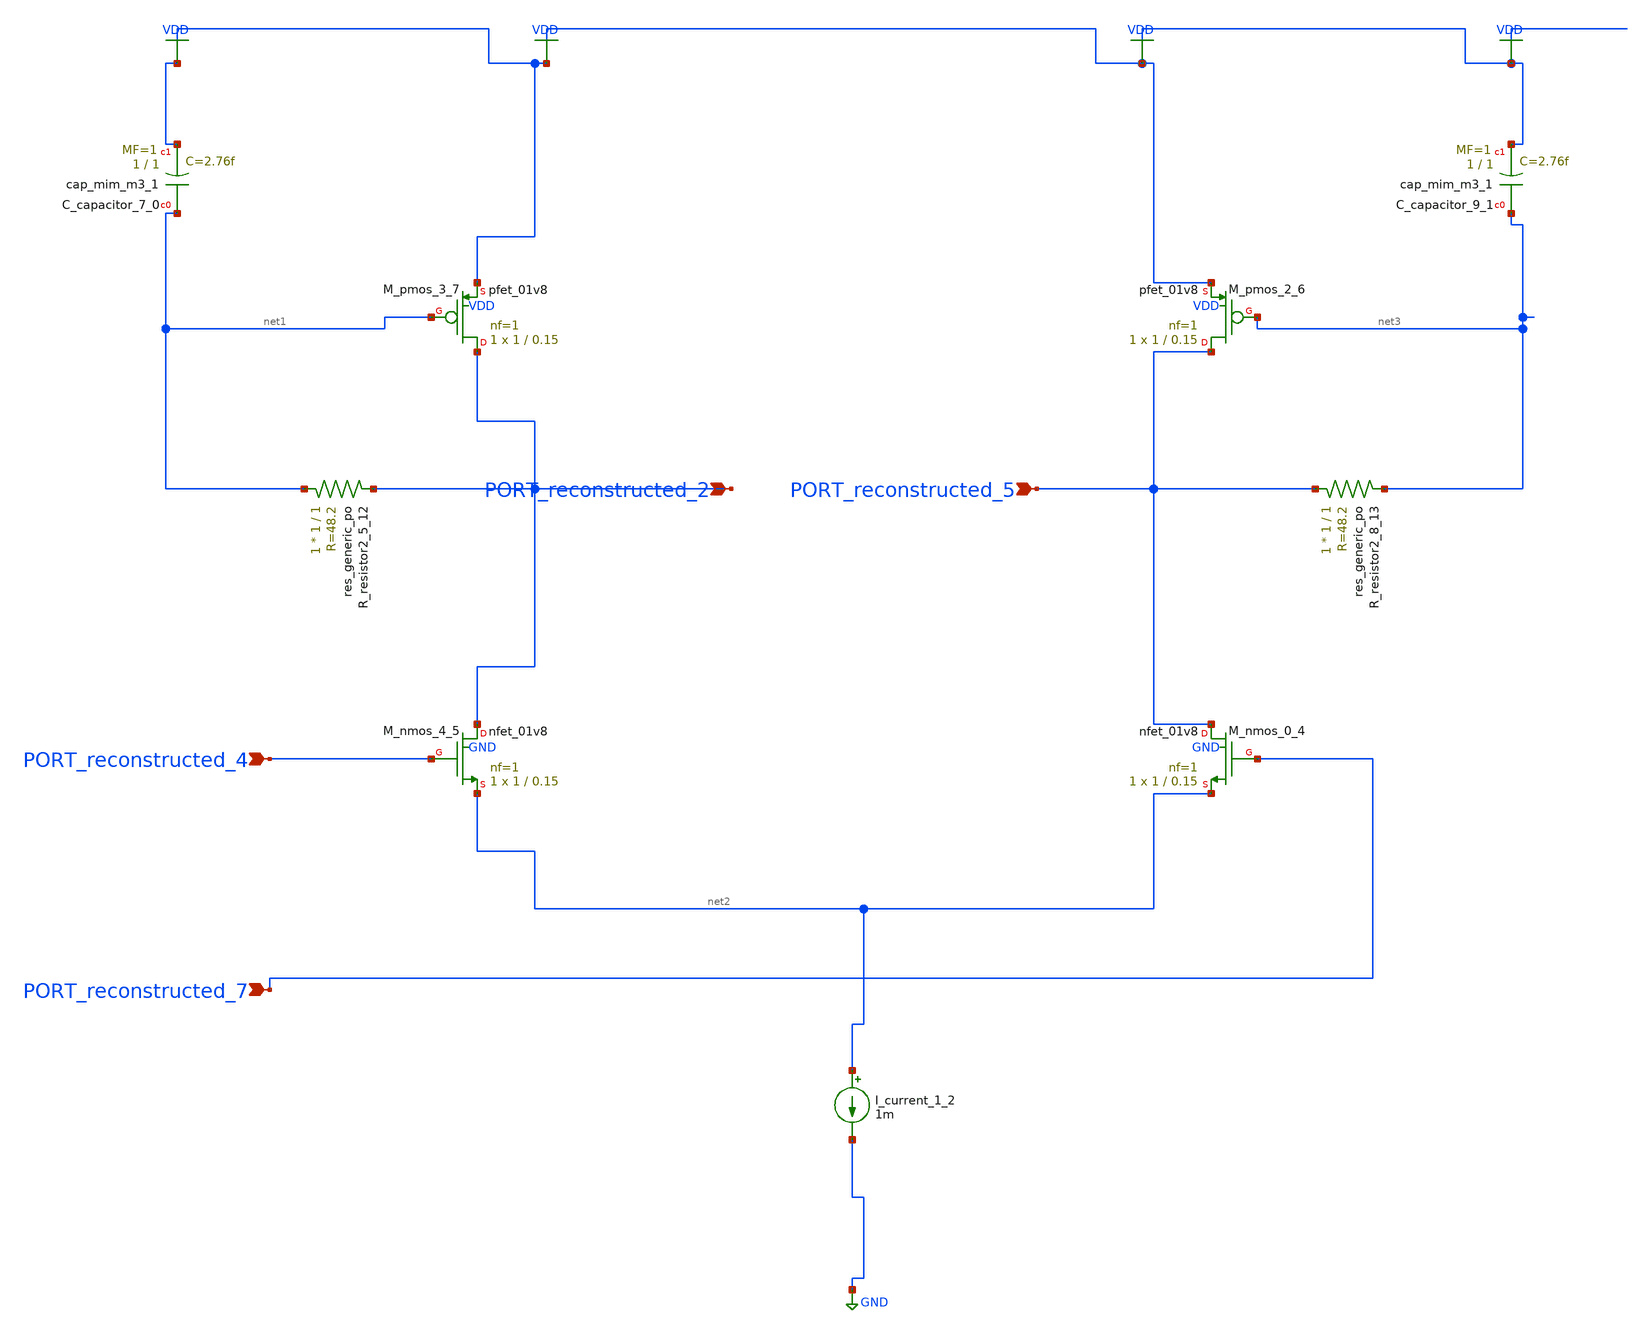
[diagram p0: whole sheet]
** sch_path: schematics/AMSNet/426.sch
**.subckt 426 PORT_reconstructed_2 PORT_reconstructed_5 PORT_reconstructed_4 PORT_reconstructed_7
*.ipin PORT_reconstructed_2
*.ipin PORT_reconstructed_5
*.ipin PORT_reconstructed_4
*.ipin PORT_reconstructed_7
XC_capacitor_7_0 net1 VDD sky130_fd_pr__cap_mim_m3_1 W=1 L=1 MF=1 m=1
XC_capacitor_9_1 net3 VDD sky130_fd_pr__cap_mim_m3_1 W=1 L=1 MF=1 m=1
I_current_1_2 net2 GND 1m
XM_nmos_0_4 PORT_reconstructed_5 PORT_reconstructed_7 net2 GND sky130_fd_pr__nfet_01v8 L=0.15 W=1 nf=1
+ ad='int((1 + 1)/2) * 1 / 1 * 0.29' as='int((1 + 2)/2) * 1 / 1 * 0.29' pd='2*int((1 + 1)/2) * (1 / 1 + 0.29)'
+ ps='2*int((1 + 2)/2) * (1 / 1 + 0.29)' nrd='0.29 / 1 ' nrs='0.29 / 1 ' sa=0 sb=0 sd=0 mult=1 m=1
XM_nmos_4_5 PORT_reconstructed_2 PORT_reconstructed_4 net2 GND sky130_fd_pr__nfet_01v8 L=0.15 W=1 nf=1
+ ad='int((1 + 1)/2) * 1 / 1 * 0.29' as='int((1 + 2)/2) * 1 / 1 * 0.29' pd='2*int((1 + 1)/2) * (1 / 1 + 0.29)'
+ ps='2*int((1 + 2)/2) * (1 / 1 + 0.29)' nrd='0.29 / 1 ' nrs='0.29 / 1 ' sa=0 sb=0 sd=0 mult=1 m=1
XM_pmos_2_6 PORT_reconstructed_5 net3 VDD VDD sky130_fd_pr__pfet_01v8 L=0.15 W=1 nf=1 ad='int((1 + 1)/2) * 1 / 1 * 0.29'
+ as='int((1 + 2)/2) * 1 / 1 * 0.29' pd='2*int((1 + 1)/2) * (1 / 1 + 0.29)' ps='2*int((1 + 2)/2) * (1 / 1 + 0.29)'
+ nrd='0.29 / 1 ' nrs='0.29 / 1 ' sa=0 sb=0 sd=0 mult=1 m=1
XM_pmos_3_7 PORT_reconstructed_2 net1 VDD VDD sky130_fd_pr__pfet_01v8 L=0.15 W=1 nf=1 ad='int((1 + 1)/2) * 1 / 1 * 0.29'
+ as='int((1 + 2)/2) * 1 / 1 * 0.29' pd='2*int((1 + 1)/2) * (1 / 1 + 0.29)' ps='2*int((1 + 2)/2) * (1 / 1 + 0.29)'
+ nrd='0.29 / 1 ' nrs='0.29 / 1 ' sa=0 sb=0 sd=0 mult=1 m=1
XR_resistor2_5_12 net1 PORT_reconstructed_2 sky130_fd_pr__res_generic_po W=1 L=1 m=1
XR_resistor2_8_13 PORT_reconstructed_5 net3 sky130_fd_pr__res_generic_po W=1 L=1 m=1
**.ends
.GLOBAL GND
.GLOBAL VDD
.end
